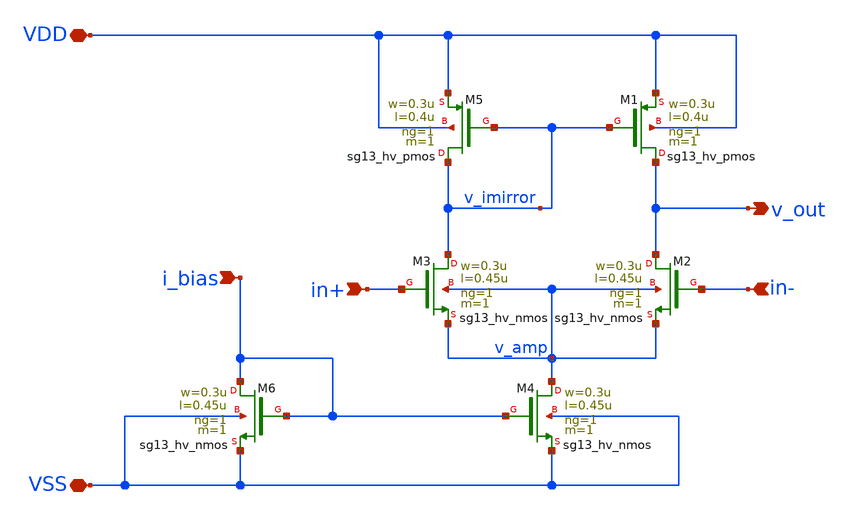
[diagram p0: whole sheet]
** sch_path: 3_Real_Cir/self_build_opamp.sch
**.subckt self_build_opamp in+ in- v_out VDD VSS i_bias
*.ipin in+
*.ipin in-
*.opin v_out
*.iopin VDD
*.iopin VSS
*.ipin i_bias
XM3 v_imirror in+ v_amp v_amp sg13_hv_nmos w=0.3u l=0.45u ng=1 m=1 mm_ok=1
XM2 v_out in- v_amp v_amp sg13_hv_nmos w=0.3u l=0.45u ng=1 m=1 mm_ok=1
XM4 v_amp i_bias VSS VSS sg13_hv_nmos w=0.3u l=0.45u ng=1 m=1 mm_ok=1
XM5 v_imirror v_imirror VDD VDD sg13_hv_pmos w=0.3u l=0.4u ng=1 m=1 mm_ok=1
XM1 v_out v_imirror VDD VDD sg13_hv_pmos w=0.3u l=0.4u ng=1 m=1 mm_ok=1
XM6 i_bias i_bias VSS VSS sg13_hv_nmos w=0.3u l=0.45u ng=1 m=1 mm_ok=1
**.ends
.end
